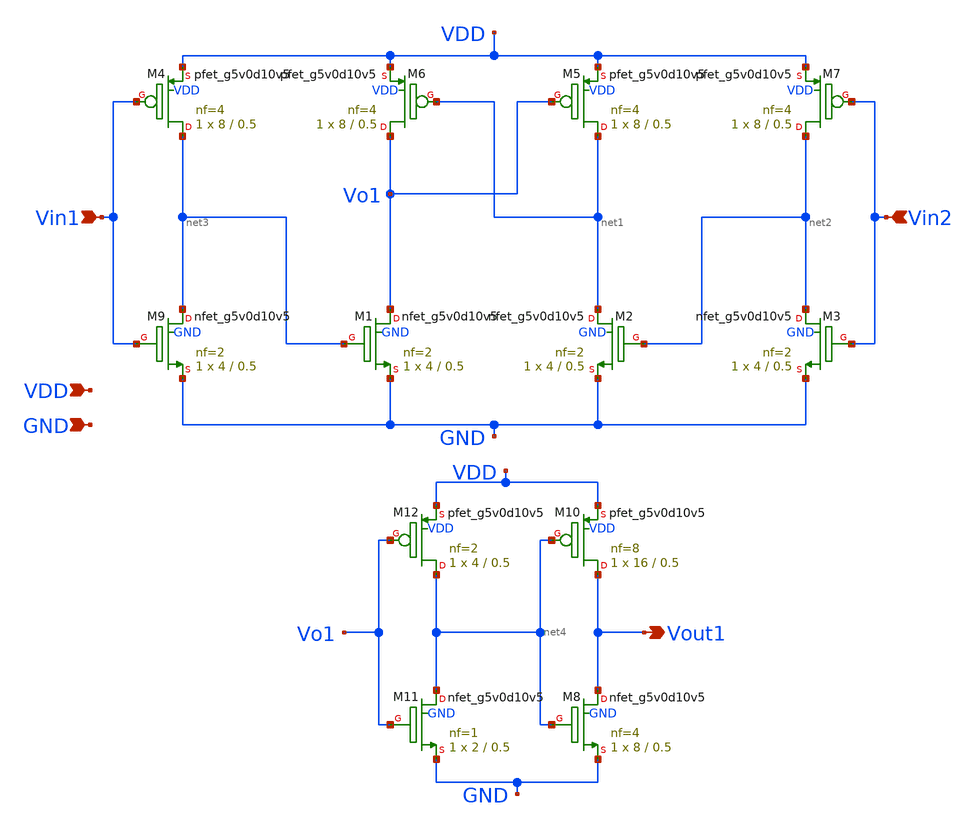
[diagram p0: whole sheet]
** sch_path: SR_3.3.sch
**.subckt SR_3.3 Vin1 Vin2 VDD GND Vout1
*.ipin Vin1
*.ipin Vin2
*.ipin VDD
*.ipin GND
*.opin Vout1
XM9 net3 Vin1 GND GND sky130_fd_pr__nfet_g5v0d10v5 L=0.5 W=4 nf=2 ad='int((nf+1)/2) * W/nf * 0.29' as='int((nf+2)/2) * W/nf * 0.29'
+ pd='2*int((nf+1)/2) * (W/nf + 0.29)' ps='2*int((nf+2)/2) * (W/nf + 0.29)' nrd='0.29 / W' nrs='0.29 / W'
+ sa=0 sb=0 sd=0 mult=1 m=1
XM1 Vo1 net3 GND GND sky130_fd_pr__nfet_g5v0d10v5 L=0.5 W=4 nf=2 ad='int((nf+1)/2) * W/nf * 0.29' as='int((nf+2)/2) * W/nf * 0.29'
+ pd='2*int((nf+1)/2) * (W/nf + 0.29)' ps='2*int((nf+2)/2) * (W/nf + 0.29)' nrd='0.29 / W' nrs='0.29 / W'
+ sa=0 sb=0 sd=0 mult=1 m=1
XM2 net1 net2 GND GND sky130_fd_pr__nfet_g5v0d10v5 L=0.5 W=4 nf=2 ad='int((nf+1)/2) * W/nf * 0.29' as='int((nf+2)/2) * W/nf * 0.29'
+ pd='2*int((nf+1)/2) * (W/nf + 0.29)' ps='2*int((nf+2)/2) * (W/nf + 0.29)' nrd='0.29 / W' nrs='0.29 / W'
+ sa=0 sb=0 sd=0 mult=1 m=1
XM3 net2 Vin2 GND GND sky130_fd_pr__nfet_g5v0d10v5 L=0.5 W=4 nf=2 ad='int((nf+1)/2) * W/nf * 0.29' as='int((nf+2)/2) * W/nf * 0.29'
+ pd='2*int((nf+1)/2) * (W/nf + 0.29)' ps='2*int((nf+2)/2) * (W/nf + 0.29)' nrd='0.29 / W' nrs='0.29 / W'
+ sa=0 sb=0 sd=0 mult=1 m=1
XM4 net3 Vin1 VDD VDD sky130_fd_pr__pfet_g5v0d10v5 L=0.5 W=8 nf=4 ad='int((nf+1)/2) * W/nf * 0.29' as='int((nf+2)/2) * W/nf * 0.29'
+ pd='2*int((nf+1)/2) * (W/nf + 0.29)' ps='2*int((nf+2)/2) * (W/nf + 0.29)' nrd='0.29 / W' nrs='0.29 / W'
+ sa=0 sb=0 sd=0 mult=1 m=1
XM5 net1 Vo1 VDD VDD sky130_fd_pr__pfet_g5v0d10v5 L=0.5 W=8 nf=4 ad='int((nf+1)/2) * W/nf * 0.29' as='int((nf+2)/2) * W/nf * 0.29'
+ pd='2*int((nf+1)/2) * (W/nf + 0.29)' ps='2*int((nf+2)/2) * (W/nf + 0.29)' nrd='0.29 / W' nrs='0.29 / W'
+ sa=0 sb=0 sd=0 mult=1 m=1
XM6 Vo1 net1 VDD VDD sky130_fd_pr__pfet_g5v0d10v5 L=0.5 W=8 nf=4 ad='int((nf+1)/2) * W/nf * 0.29' as='int((nf+2)/2) * W/nf * 0.29'
+ pd='2*int((nf+1)/2) * (W/nf + 0.29)' ps='2*int((nf+2)/2) * (W/nf + 0.29)' nrd='0.29 / W' nrs='0.29 / W'
+ sa=0 sb=0 sd=0 mult=1 m=1
XM7 net2 Vin2 VDD VDD sky130_fd_pr__pfet_g5v0d10v5 L=0.5 W=8 nf=4 ad='int((nf+1)/2) * W/nf * 0.29' as='int((nf+2)/2) * W/nf * 0.29'
+ pd='2*int((nf+1)/2) * (W/nf + 0.29)' ps='2*int((nf+2)/2) * (W/nf + 0.29)' nrd='0.29 / W' nrs='0.29 / W'
+ sa=0 sb=0 sd=0 mult=1 m=1
XM8 Vout1 net4 GND GND sky130_fd_pr__nfet_g5v0d10v5 L=0.5 W=8 nf=4 ad='int((nf+1)/2) * W/nf * 0.29' as='int((nf+2)/2) * W/nf * 0.29'
+ pd='2*int((nf+1)/2) * (W/nf + 0.29)' ps='2*int((nf+2)/2) * (W/nf + 0.29)' nrd='0.29 / W' nrs='0.29 / W'
+ sa=0 sb=0 sd=0 mult=1 m=1
XM10 Vout1 net4 VDD VDD sky130_fd_pr__pfet_g5v0d10v5 L=0.5 W=16 nf=8 ad='int((nf+1)/2) * W/nf * 0.29'
+ as='int((nf+2)/2) * W/nf * 0.29' pd='2*int((nf+1)/2) * (W/nf + 0.29)' ps='2*int((nf+2)/2) * (W/nf + 0.29)'
+ nrd='0.29 / W' nrs='0.29 / W' sa=0 sb=0 sd=0 mult=1 m=1
XM11 net4 Vo1 GND GND sky130_fd_pr__nfet_g5v0d10v5 L=0.5 W=2 nf=1 ad='int((nf+1)/2) * W/nf * 0.29' as='int((nf+2)/2) * W/nf * 0.29'
+ pd='2*int((nf+1)/2) * (W/nf + 0.29)' ps='2*int((nf+2)/2) * (W/nf + 0.29)' nrd='0.29 / W' nrs='0.29 / W'
+ sa=0 sb=0 sd=0 mult=1 m=1
XM12 net4 Vo1 VDD VDD sky130_fd_pr__pfet_g5v0d10v5 L=0.5 W=4 nf=2 ad='int((nf+1)/2) * W/nf * 0.29' as='int((nf+2)/2) * W/nf * 0.29'
+ pd='2*int((nf+1)/2) * (W/nf + 0.29)' ps='2*int((nf+2)/2) * (W/nf + 0.29)' nrd='0.29 / W' nrs='0.29 / W'
+ sa=0 sb=0 sd=0 mult=1 m=1
**.ends
.end
